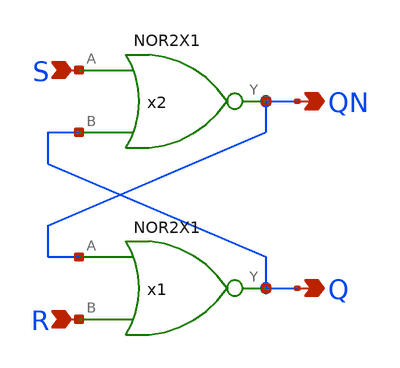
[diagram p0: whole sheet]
** sch_path: lib/xschem/SRLATCH.sch
**.subckt SRLATCH S R QN Q
*.ipin S
*.ipin R
*.opin QN
*.opin Q
x1 Q QN R NOR2X1
x2 QN S Q NOR2X1
**.ends

* expanding   symbol:  NOR2X1.sym # of pins=3
** sym_path: lib/xschem/NOR2X1.sym
** sch_path: lib/xschem/NOR2X1.sch
.subckt NOR2X1 Y A B
*.opin Y
*.ipin A
*.ipin B
XM1 Y A VSS VSS sky130_fd_pr__nfet_01v8 L=0.15 W=3 nf=1 ad='int((nf+1)/2) * W/nf * 0.29' as='int((nf+2)/2) * W/nf * 0.29'
+ pd='2*int((nf+1)/2) * (W/nf + 0.29)' ps='2*int((nf+2)/2) * (W/nf + 0.29)' nrd='0.29 / W' nrs='0.29 / W'
+ sa=0 sb=0 sd=0 mult=1 m=1
XM2 net1 A VDD VDD sky130_fd_pr__pfet_01v8 L=0.15 W=2 nf=1 ad='int((nf+1)/2) * W/nf * 0.29' as='int((nf+2)/2) * W/nf * 0.29'
+ pd='2*int((nf+1)/2) * (W/nf + 0.29)' ps='2*int((nf+2)/2) * (W/nf + 0.29)' nrd='0.29 / W' nrs='0.29 / W'
+ sa=0 sb=0 sd=0 mult=2 m=2
XM3 Y B VSS VSS sky130_fd_pr__nfet_01v8 L=0.15 W=3 nf=1 ad='int((nf+1)/2) * W/nf * 0.29' as='int((nf+2)/2) * W/nf * 0.29'
+ pd='2*int((nf+1)/2) * (W/nf + 0.29)' ps='2*int((nf+2)/2) * (W/nf + 0.29)' nrd='0.29 / W' nrs='0.29 / W'
+ sa=0 sb=0 sd=0 mult=1 m=1
XM5 Y B net1 VDD sky130_fd_pr__pfet_01v8 L=0.15 W=2 nf=1 ad='int((nf+1)/2) * W/nf * 0.29' as='int((nf+2)/2) * W/nf * 0.29'
+ pd='2*int((nf+1)/2) * (W/nf + 0.29)' ps='2*int((nf+2)/2) * (W/nf + 0.29)' nrd='0.29 / W' nrs='0.29 / W'
+ sa=0 sb=0 sd=0 mult=2 m=2
.ends

.end
